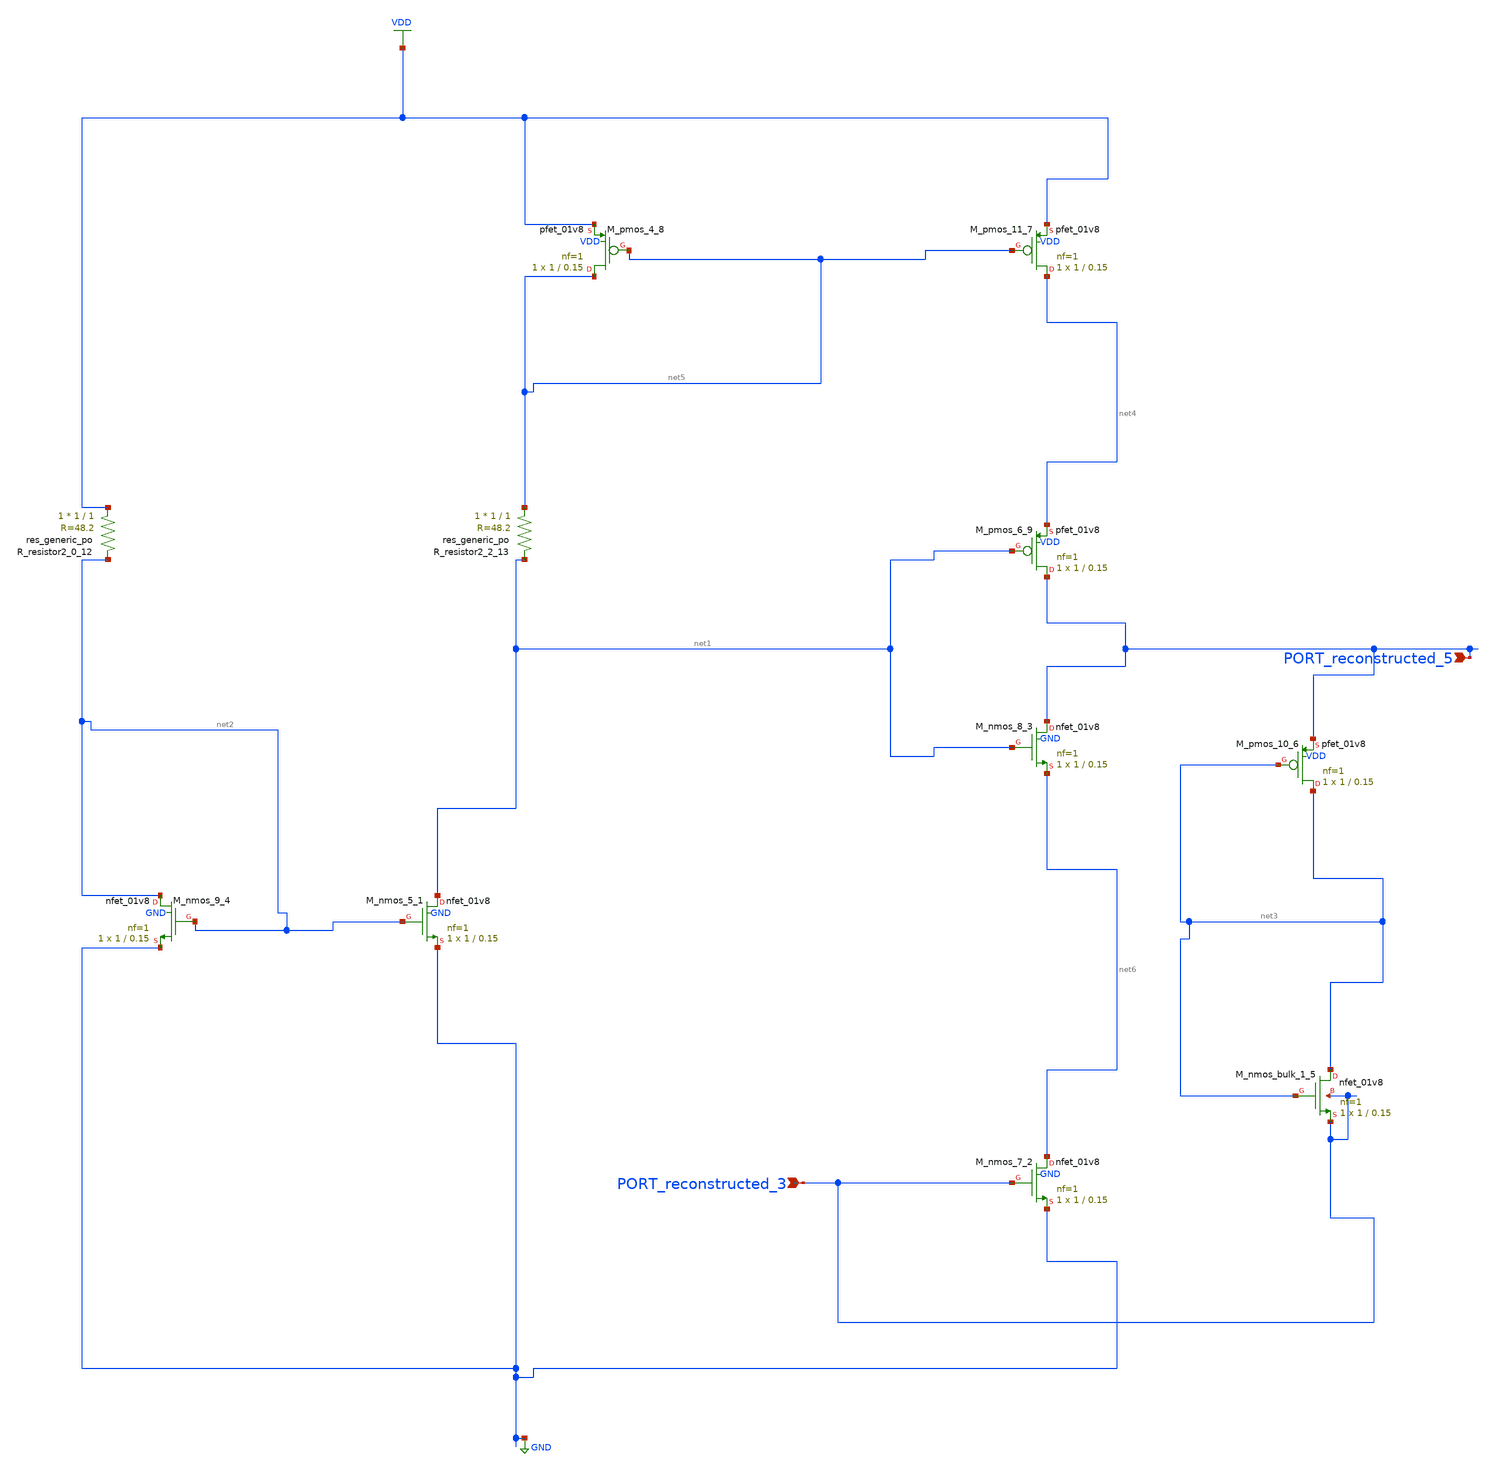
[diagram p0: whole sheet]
** sch_path: schematics/SchemGen/10_1371_journal_pone_0158954_07_001.sch
**.subckt 10_1371_journal_pone_0158954_07_001 PORT_reconstructed_3 PORT_reconstructed_5
*.ipin PORT_reconstructed_3
*.ipin PORT_reconstructed_5
XM_nmos_5_1 net1 net2 GND GND sky130_fd_pr__nfet_01v8 L=0.15 W=1 nf=1 ad='int((1 + 1)/2) * 1 / 1 * 0.29'
+ as='int((1 + 2)/2) * 1 / 1 * 0.29' pd='2*int((1 + 1)/2) * (1 / 1 + 0.29)' ps='2*int((1 + 2)/2) * (1 / 1 + 0.29)'
+ nrd='0.29 / 1 ' nrs='0.29 / 1 ' sa=0 sb=0 sd=0 mult=1 m=1
XM_nmos_7_2 net6 PORT_reconstructed_3 GND GND sky130_fd_pr__nfet_01v8 L=0.15 W=1 nf=1 ad='int((1 + 1)/2) * 1 / 1 * 0.29'
+ as='int((1 + 2)/2) * 1 / 1 * 0.29' pd='2*int((1 + 1)/2) * (1 / 1 + 0.29)' ps='2*int((1 + 2)/2) * (1 / 1 + 0.29)'
+ nrd='0.29 / 1 ' nrs='0.29 / 1 ' sa=0 sb=0 sd=0 mult=1 m=1
XM_nmos_8_3 PORT_reconstructed_5 net1 net6 GND sky130_fd_pr__nfet_01v8 L=0.15 W=1 nf=1 ad='int((1 + 1)/2) * 1 / 1 * 0.29'
+ as='int((1 + 2)/2) * 1 / 1 * 0.29' pd='2*int((1 + 1)/2) * (1 / 1 + 0.29)' ps='2*int((1 + 2)/2) * (1 / 1 + 0.29)'
+ nrd='0.29 / 1 ' nrs='0.29 / 1 ' sa=0 sb=0 sd=0 mult=1 m=1
XM_nmos_9_4 net2 net2 GND GND sky130_fd_pr__nfet_01v8 L=0.15 W=1 nf=1 ad='int((1 + 1)/2) * 1 / 1 * 0.29'
+ as='int((1 + 2)/2) * 1 / 1 * 0.29' pd='2*int((1 + 1)/2) * (1 / 1 + 0.29)' ps='2*int((1 + 2)/2) * (1 / 1 + 0.29)'
+ nrd='0.29 / 1 ' nrs='0.29 / 1 ' sa=0 sb=0 sd=0 mult=1 m=1
XM_nmos_bulk_1_5 net3 net3 PORT_reconstructed_3 PORT_reconstructed_3 sky130_fd_pr__nfet_01v8 L=0.15 W=1
+ nf=1 ad='int((1 + 1)/2) * 1 / 1 * 0.29' as='int((1 + 2)/2) * 1 / 1 * 0.29' pd='2*int((1 + 1)/2) * (1 / 1 + 0.29)'
+ ps='2*int((1 + 2)/2) * (1 / 1 + 0.29)' nrd='0.29 / 1 ' nrs='0.29 / 1 ' sa=0 sb=0 sd=0 mult=1 m=1
XM_pmos_10_6 net3 net3 PORT_reconstructed_5 VDD sky130_fd_pr__pfet_01v8 L=0.15 W=1 nf=1 ad='int((1 + 1)/2) * 1 / 1 * 0.29'
+ as='int((1 + 2)/2) * 1 / 1 * 0.29' pd='2*int((1 + 1)/2) * (1 / 1 + 0.29)' ps='2*int((1 + 2)/2) * (1 / 1 + 0.29)'
+ nrd='0.29 / 1 ' nrs='0.29 / 1 ' sa=0 sb=0 sd=0 mult=1 m=1
XM_pmos_11_7 net4 net5 VDD VDD sky130_fd_pr__pfet_01v8 L=0.15 W=1 nf=1 ad='int((1 + 1)/2) * 1 / 1 * 0.29'
+ as='int((1 + 2)/2) * 1 / 1 * 0.29' pd='2*int((1 + 1)/2) * (1 / 1 + 0.29)' ps='2*int((1 + 2)/2) * (1 / 1 + 0.29)'
+ nrd='0.29 / 1 ' nrs='0.29 / 1 ' sa=0 sb=0 sd=0 mult=1 m=1
XM_pmos_4_8 net5 net5 VDD VDD sky130_fd_pr__pfet_01v8 L=0.15 W=1 nf=1 ad='int((1 + 1)/2) * 1 / 1 * 0.29'
+ as='int((1 + 2)/2) * 1 / 1 * 0.29' pd='2*int((1 + 1)/2) * (1 / 1 + 0.29)' ps='2*int((1 + 2)/2) * (1 / 1 + 0.29)'
+ nrd='0.29 / 1 ' nrs='0.29 / 1 ' sa=0 sb=0 sd=0 mult=1 m=1
XM_pmos_6_9 PORT_reconstructed_5 net1 net4 VDD sky130_fd_pr__pfet_01v8 L=0.15 W=1 nf=1 ad='int((1 + 1)/2) * 1 / 1 * 0.29'
+ as='int((1 + 2)/2) * 1 / 1 * 0.29' pd='2*int((1 + 1)/2) * (1 / 1 + 0.29)' ps='2*int((1 + 2)/2) * (1 / 1 + 0.29)'
+ nrd='0.29 / 1 ' nrs='0.29 / 1 ' sa=0 sb=0 sd=0 mult=1 m=1
XR_resistor2_0_12 VDD net2 sky130_fd_pr__res_generic_po W=1 L=1 m=1
XR_resistor2_2_13 net5 net1 sky130_fd_pr__res_generic_po W=1 L=1 m=1
**.ends
.GLOBAL GND
.GLOBAL VDD
.end
